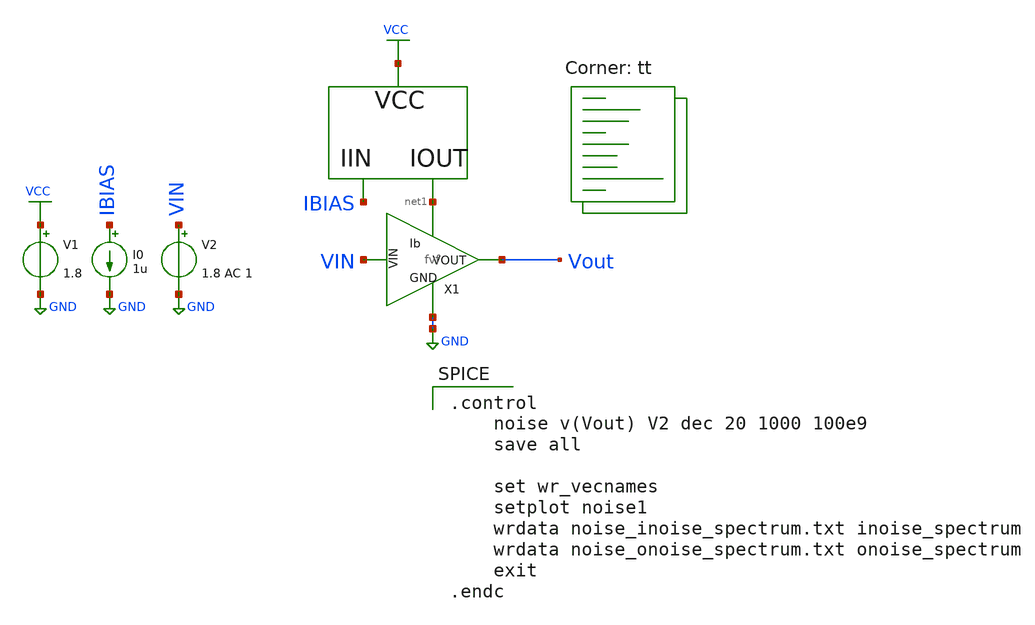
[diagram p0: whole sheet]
** sch_path: xschem/fvf_tb_noise.sch
**.subckt fvf_tb_noise
V1 VCC GND 1.8
I0 IBIAS GND 1u
X1 net1 GND VIN Vout fvf
V2 VIN GND 1.8 AC 1
**** begin user architecture code
.lib $::SKYWATER_MODELS/sky130.lib.spice tt

.control
    noise v(Vout) V2 dec 20 1000 100e9
    save all

    set wr_vecnames
    setplot noise1
    wrdata noise_inoise_spectrum.txt inoise_spectrum
    wrdata noise_onoise_spectrum.txt onoise_spectrum
    exit
.endc

**** end user architecture code
**.ends

* expanding   symbol:  /foss/designs/fvf-chipathon-2024/xschem/fvf.sym # of pins=4
** sym_path: xschem/fvf.sym
** sch_path: xschem/fvf.sch
.subckt fvf Ib GND VIN VOUT
*.ipin VIN
*.opin VOUT
*.iopin GND
*.ipin Ib
XM1 Ib VIN VOUT GND sky130_fd_pr__nfet_01v8 L=1 W=15 nf=1 ad='int((nf+1)/2) * W/nf * 0.29' as='int((nf+2)/2) * W/nf * 0.29'
+ pd='2*int((nf+1)/2) * (W/nf + 0.29)' ps='2*int((nf+2)/2) * (W/nf + 0.29)' nrd='0.29 / W' nrs='0.29 / W'
+ sa=0 sb=0 sd=0 mult=1 m=1
XM2 VOUT Ib GND GND sky130_fd_pr__nfet_01v8 L=1 W=15 nf=1 ad='int((nf+1)/2) * W/nf * 0.29' as='int((nf+2)/2) * W/nf * 0.29'
+ pd='2*int((nf+1)/2) * (W/nf + 0.29)' ps='2*int((nf+2)/2) * (W/nf + 0.29)' nrd='0.29 / W' nrs='0.29 / W'
+ sa=0 sb=0 sd=0 mult=1 m=1
.ends

.GLOBAL GND
.GLOBAL VCC
.end
